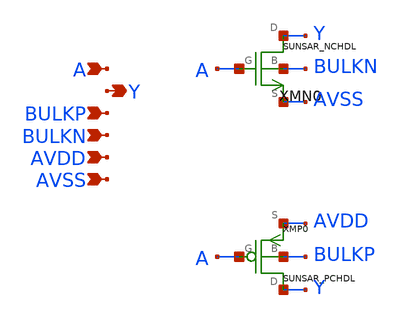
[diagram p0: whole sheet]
** sch_path: ip/sun_sar9b_sky130nm/design/SUN_SAR9B_SKY130NM/SUNSAR_IVX1_CV.sch
**.subckt SUNSAR_IVX1_CV A Y BULKP BULKN AVDD AVSS
*.ipin A
*.opin Y
*.ipin BULKP
*.ipin BULKN
*.ipin AVDD
*.ipin AVSS
XMN0 Y A AVSS BULKN SUNSAR_NCHDL
XMP0 Y A AVDD BULKP SUNSAR_PCHDL
**.ends
.end
